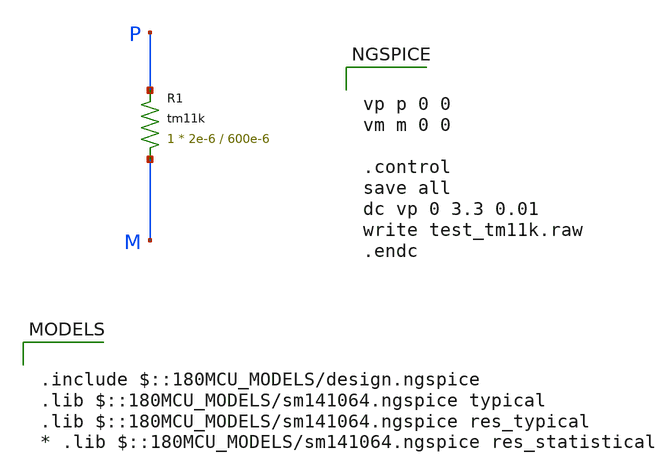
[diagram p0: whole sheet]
** sch_path: cells/xschem/tests/test_tm11k.sch
**.subckt test_tm11k
XR1 M P tm11k r_width=2e-6 r_length=600e-6 m=1
**** begin user architecture code

.include $::180MCU_MODELS/design.ngspice
.lib $::180MCU_MODELS/sm141064.ngspice typical
.lib $::180MCU_MODELS/sm141064.ngspice res_typical
* .lib $::180MCU_MODELS/sm141064.ngspice res_statistical



vp p 0 0
vm m 0 0

.control
save all
dc vp 0 3.3 0.01
write test_tm11k.raw
.endc


**** end user architecture code
**.ends
.end
